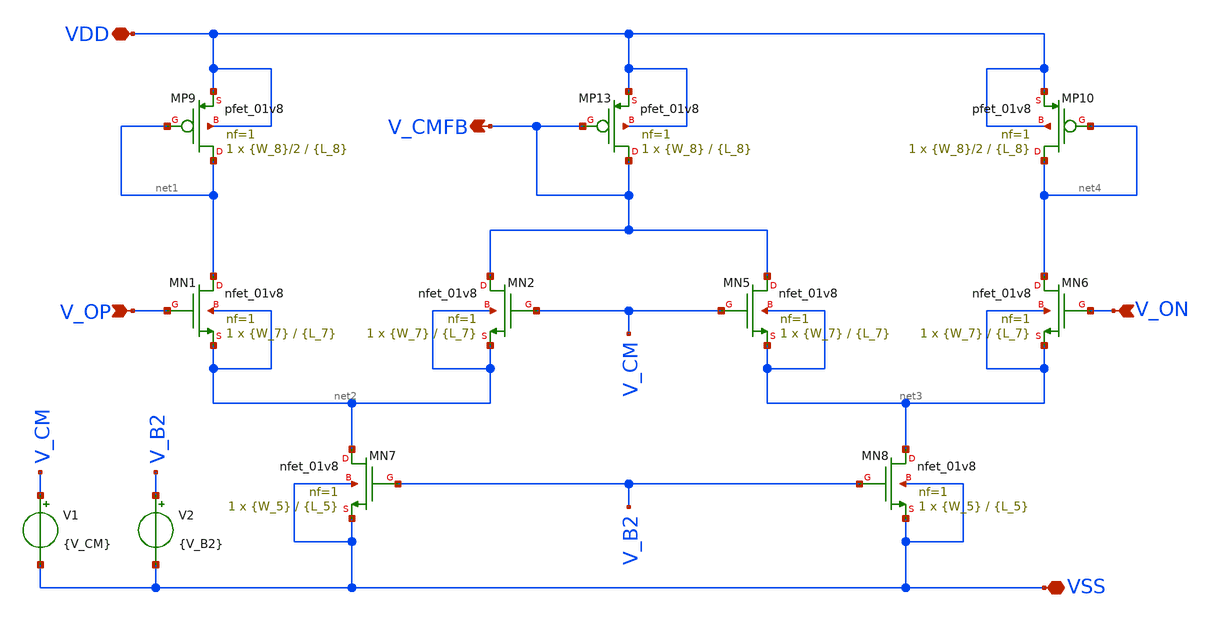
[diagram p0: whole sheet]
** sch_path: Xschem Simulations/FDDA_CMFB/CMFB.sch
**.subckt CMFB V_CMFB V_OP V_ON VSS VDD
*.opin V_CMFB
*.ipin V_OP
*.ipin V_ON
*.iopin VSS
*.iopin VDD
XMN1 net1 V_OP net2 net2 sky130_fd_pr__nfet_01v8 L={L_7} W={W_7} nf=1 ad='int((1 + 1)/2) * {W_7} / 1 * 0.29'
+ as='int((1 + 2)/2) * {W_7} / 1 * 0.29' pd='2*int((1 + 1)/2) * ({W_7} / 1 + 0.29)' ps='2*int((1 + 2)/2) * ({W_7} / 1 + 0.29)'
+ nrd='0.29 / {W_7} ' nrs='0.29 / {W_7} ' sa=0 sb=0 sd=0 mult=1 m=1
XMN2 V_CMFB V_CM net2 net2 sky130_fd_pr__nfet_01v8 L={L_7} W={W_7} nf=1 ad='int((1 + 1)/2) * {W_7} / 1 * 0.29'
+ as='int((1 + 2)/2) * {W_7} / 1 * 0.29' pd='2*int((1 + 1)/2) * ({W_7} / 1 + 0.29)' ps='2*int((1 + 2)/2) * ({W_7} / 1 + 0.29)'
+ nrd='0.29 / {W_7} ' nrs='0.29 / {W_7} ' sa=0 sb=0 sd=0 mult=1 m=1
XMN7 net2 V_B2 VSS VSS sky130_fd_pr__nfet_01v8 L={L_5} W={W_5} nf=1 ad='int((1 + 1)/2) * {W_5} / 1 * 0.29'
+ as='int((1 + 2)/2) * {W_5} / 1 * 0.29' pd='2*int((1 + 1)/2) * ({W_5} / 1 + 0.29)' ps='2*int((1 + 2)/2) * ({W_5} / 1 + 0.29)'
+ nrd='0.29 / {W_5} ' nrs='0.29 / {W_5} ' sa=0 sb=0 sd=0 mult=1 m=1
XMN6 net4 V_ON net3 net3 sky130_fd_pr__nfet_01v8 L={L_7} W={W_7} nf=1 ad='int((1 + 1)/2) * {W_7} / 1 * 0.29'
+ as='int((1 + 2)/2) * {W_7} / 1 * 0.29' pd='2*int((1 + 1)/2) * ({W_7} / 1 + 0.29)' ps='2*int((1 + 2)/2) * ({W_7} / 1 + 0.29)'
+ nrd='0.29 / {W_7} ' nrs='0.29 / {W_7} ' sa=0 sb=0 sd=0 mult=1 m=1
XMN5 V_CMFB V_CM net3 net3 sky130_fd_pr__nfet_01v8 L={L_7} W={W_7} nf=1 ad='int((1 + 1)/2) * {W_7} / 1 * 0.29'
+ as='int((1 + 2)/2) * {W_7} / 1 * 0.29' pd='2*int((1 + 1)/2) * ({W_7} / 1 + 0.29)' ps='2*int((1 + 2)/2) * ({W_7} / 1 + 0.29)'
+ nrd='0.29 / {W_7} ' nrs='0.29 / {W_7} ' sa=0 sb=0 sd=0 mult=1 m=1
XMN8 net3 V_B2 VSS VSS sky130_fd_pr__nfet_01v8 L={L_5} W={W_5} nf=1 ad='int((1 + 1)/2) * {W_5} / 1 * 0.29'
+ as='int((1 + 2)/2) * {W_5} / 1 * 0.29' pd='2*int((1 + 1)/2) * ({W_5} / 1 + 0.29)' ps='2*int((1 + 2)/2) * ({W_5} / 1 + 0.29)'
+ nrd='0.29 / {W_5} ' nrs='0.29 / {W_5} ' sa=0 sb=0 sd=0 mult=1 m=1
XMP9 net1 net1 VDD VDD sky130_fd_pr__pfet_01v8 L={L_8} W={W_8}/2 nf=1 ad='int((1 + 1)/2) * {W_8}/2 / 1 * 0.29'
+ as='int((1 + 2)/2) * {W_8}/2 / 1 * 0.29' pd='2*int((1 + 1)/2) * ({W_8}/2 / 1 + 0.29)' ps='2*int((1 + 2)/2) * ({W_8}/2 / 1 + 0.29)'
+ nrd='0.29 / {W_8}/2 ' nrs='0.29 / {W_8}/2 ' sa=0 sb=0 sd=0 mult=1 m=1
XMP13 V_CMFB V_CMFB VDD VDD sky130_fd_pr__pfet_01v8 L={L_8} W={W_8} nf=1 ad='int((1 + 1)/2) * {W_8} / 1 * 0.29'
+ as='int((1 + 2)/2) * {W_8} / 1 * 0.29' pd='2*int((1 + 1)/2) * ({W_8} / 1 + 0.29)' ps='2*int((1 + 2)/2) * ({W_8} / 1 + 0.29)'
+ nrd='0.29 / {W_8} ' nrs='0.29 / {W_8} ' sa=0 sb=0 sd=0 mult=1 m=1
XMP10 net4 net4 VDD VDD sky130_fd_pr__pfet_01v8 L={L_8} W={W_8}/2 nf=1 ad='int((1 + 1)/2) * {W_8}/2 / 1 * 0.29'
+ as='int((1 + 2)/2) * {W_8}/2 / 1 * 0.29' pd='2*int((1 + 1)/2) * ({W_8}/2 / 1 + 0.29)' ps='2*int((1 + 2)/2) * ({W_8}/2 / 1 + 0.29)'
+ nrd='0.29 / {W_8}/2 ' nrs='0.29 / {W_8}/2 ' sa=0 sb=0 sd=0 mult=1 m=1
V2 V_B2 VSS {V_B2}
V1 V_CM VSS {V_CM}
**.ends
.end
